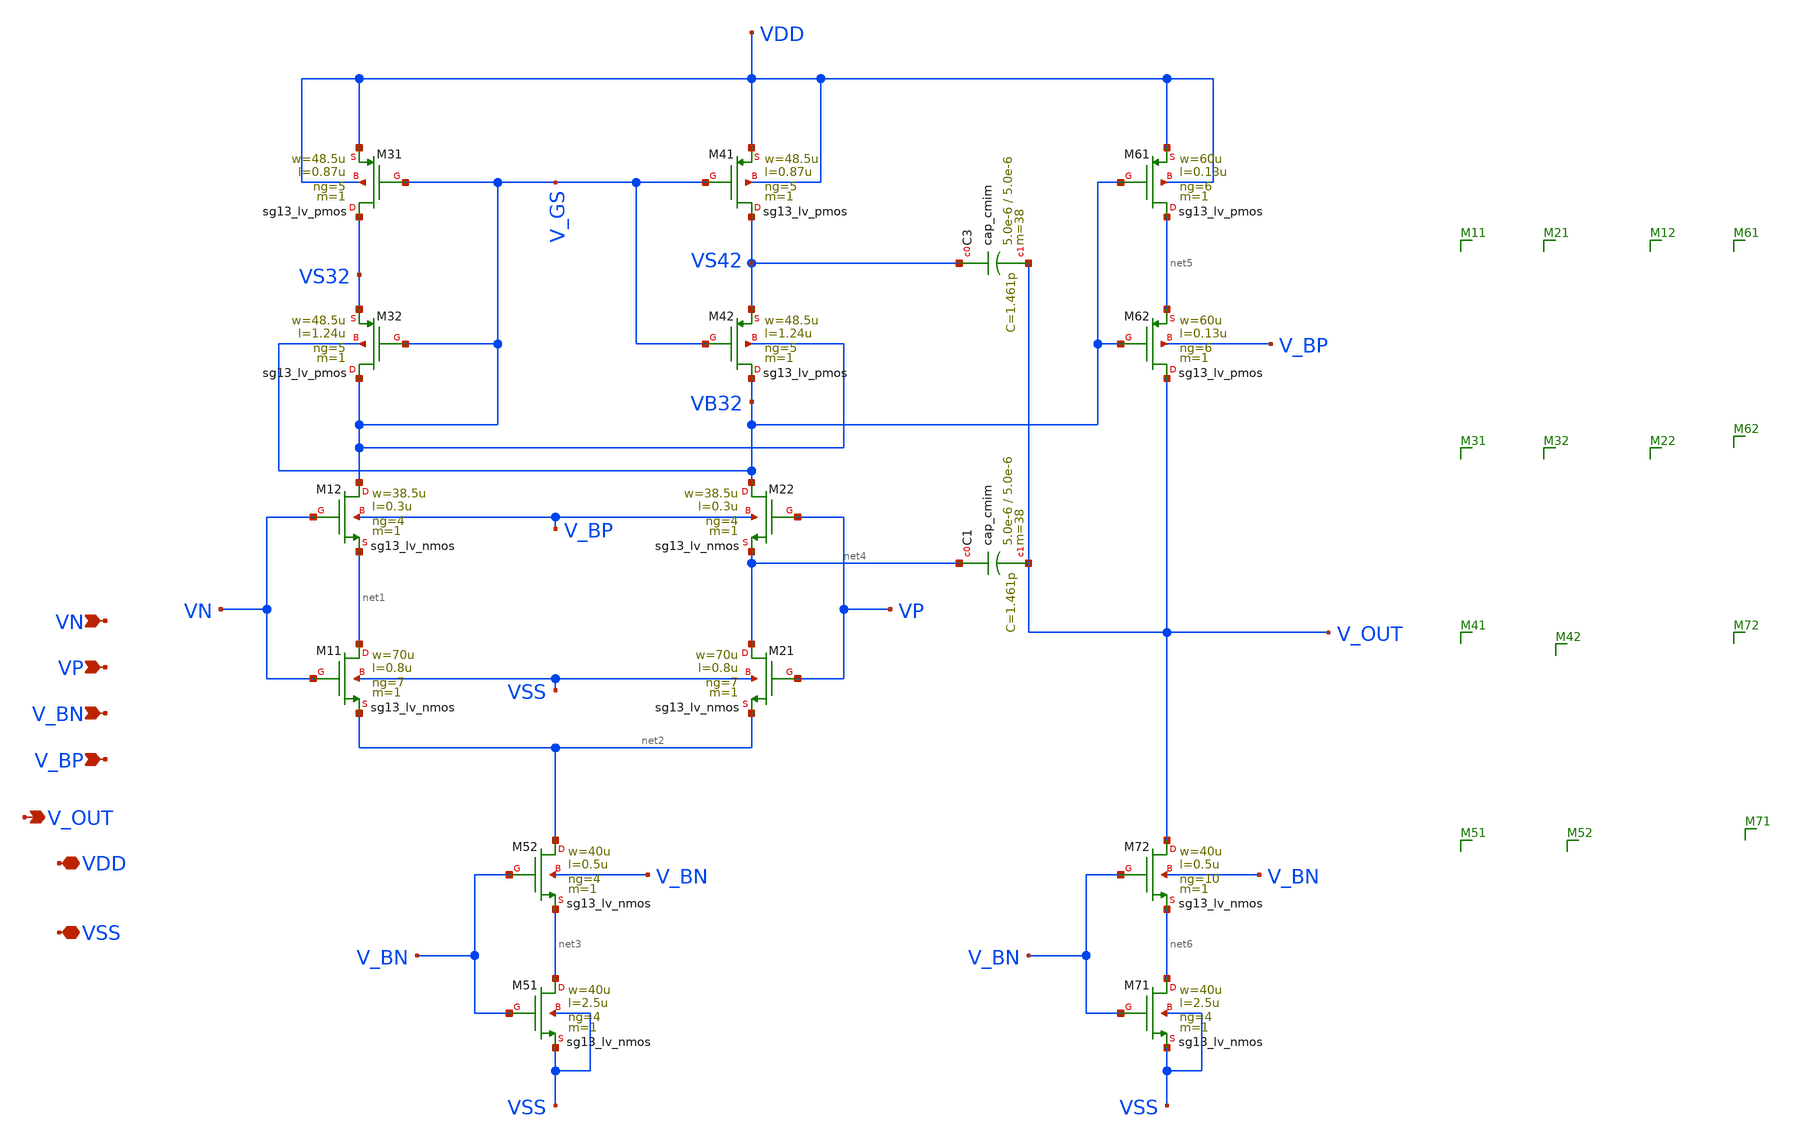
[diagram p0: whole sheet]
** sch_path: xschem/Pseudo_compensated_self_cascode_OTA.sch
**.subckt Pseudo_compensated_self_cascode_OTA VN VP V_BN V_BP V_OUT VDD VSS
*.ipin VN
*.ipin VP
*.ipin V_BN
*.ipin V_BP
*.opin V_OUT
*.iopin VDD
*.iopin VSS
XM11 net1 VN net2 VSS sg13_lv_nmos w=70u l=0.8u ng=7 m=1 mm_ok=1
XM12 V_GS VN net1 V_BP sg13_lv_nmos w=38.5u l=0.3u ng=4 m=1 mm_ok=1
XM21 net4 VP net2 VSS sg13_lv_nmos w=70u l=0.8u ng=7 m=1 mm_ok=1
XM22 VB32 VP net4 V_BP sg13_lv_nmos w=38.5u l=0.3u ng=4 m=1 mm_ok=1
XM52 net2 V_BN net3 V_BN sg13_lv_nmos w=40u l=0.5u ng=4 m=1 mm_ok=1
XM51 net3 V_BN VSS VSS sg13_lv_nmos w=40u l=2.5u ng=4 m=1 mm_ok=1
XM32 V_GS V_GS VS32 VB32 sg13_lv_pmos w=48.5u l=1.24u ng=5 m=1 mm_ok=1
XM31 VS32 V_GS VDD VDD sg13_lv_pmos w=48.5u l=0.87u ng=5 m=1 mm_ok=1
XM42 VB32 V_GS VS42 V_GS sg13_lv_pmos w=48.5u l=1.24u ng=5 m=1 mm_ok=1
XM41 VS42 V_GS VDD VDD sg13_lv_pmos w=48.5u l=0.87u ng=5 m=1 mm_ok=1
XM61 net5 VB32 VDD VDD sg13_lv_pmos w=60u l=0.13u ng=6 m=1 mm_ok=1
XM62 V_OUT VB32 net5 V_BP sg13_lv_pmos w=60u l=0.13u ng=6 m=1 mm_ok=1
XM72 V_OUT V_BN net6 V_BN sg13_lv_nmos w=40u l=0.5u ng=10 m=1 mm_ok=1
XM71 net6 V_BN VSS VSS sg13_lv_nmos w=40u l=2.5u ng=4 m=1 mm_ok=1
XC3 VS42 V_OUT cap_cmim w=5.0e-6 l=5.0e-6 m=38 mm_ok=1
XC1 net4 V_OUT cap_cmim w=5.0e-6 l=5.0e-6 m=38 mm_ok=1
**.ends
.end
